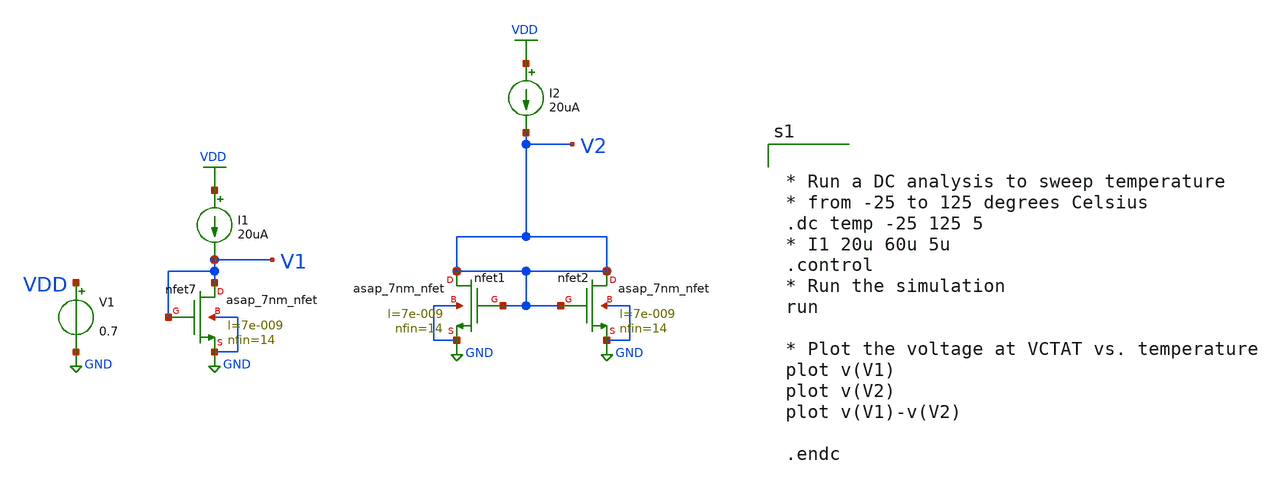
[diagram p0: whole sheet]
** sch_path: xschem/Circuits/PTAT_IDEAL_CURRENT_SOURCE.sch
* AsahiroKenpachi/asap_7nm_Xschem/asap_7nm_nfet.sym:
* Copyright 2021 Stefan Frederik Schippers
* Licensed under the Apache License, Version 2.0 (the "License");
**.subckt PTAT_IDEAL_CURRENT_SOURCE
I1 VDD V1 20uA
V1 VDD GND 0.7
Xnfet7 V1 V1 GND GND asap_7nm_nfet l=7e-009 nfin=14
I2 VDD V2 20uA
Xnfet1 V2 V2 GND GND asap_7nm_nfet l=7e-009 nfin=14
Xnfet2 V2 V2 GND GND asap_7nm_nfet l=7e-009 nfin=14
**** begin user architecture code


* Run a DC analysis to sweep temperature
* from -25 to 125 degrees Celsius
.dc temp -25 125 5
* I1 20u 60u 5u
.control
* Run the simulation
run

* Plot the voltage at VCTAT vs. temperature
plot v(V1)
plot v(V2)
plot v(V1)-v(V2)

.endc


**** end user architecture code
**.ends
.GLOBAL VDD
.GLOBAL GND
**** begin user architecture code

.subckt asap_7nm_nfet S G D B l=@l nfin=@nfin
	nnmos_finfet S G D B BSIMCMG_osdi_N l=@l nfin=@nfin
.ends asap_7nm_nfet

.model BSIMCMG_osdi_N BSIMCMG_va (  TYPE = 1
************************************************************
*                         general                          *
************************************************************ version = 107             bulkmod = 1
*+               igcmod  = 1               igbmod  = 0              gidlmod = 1               iimod   = 0
*+               geomod  = 1               rdsmod  = 0              rgatemod= 0               rgeomod = 0
*+               shmod   = 0               nqsmod  = 0              coremod = 0               cgeomod = 0
*+               capmod  = 0               tnom    = 25             eot     = 1e-009          eotbox  = 1.4e-007
*+        eotacc  = 1e-010          tfin    = 6.5e-009       toxp    = 2.1e-009        nbody   = 1e+022
*+          phig    = 4.2466          epsrox  = 3.9            epsrsub = 11.9            easub   = 4.05
*+            ni0sub  = 1.1e+016        bg0sub  = 1.17           nc0sub  = 2.86e+025       nsd     = 2e+026
*+          ngate   = 0               nseg    = 5              l       = 2.1e-008        xl      = 1e-009
*+          lint    = -2e-009         dlc     = 0              dlbin   = 0               hfin    = 3.2e-008
*+        deltaw  = 0               deltawcv= 0              sdterm  = 0               epsrsp  = 3.9
*+             nfin    = 1 toxg    = 1.80e-009
************************************************************
*                            dc                            *
************************************************************ cit     = 0               cdsc    =
*+ 0.01            cdscd   = 0.01            dvt0    = 0.05           dvt1    = 0.47            phin    =
*+ 0.05            eta0    = 0.07            dsub    = 0.35           k1rsce  = 0               lpe0    = 0
*+               dvtshift= 0               qmfactor= 2.5            etaqm   = 0.54            qm0     = 0.001           pqm
*+     = 0.66            u0      = 0.0303         etamob  = 2               up      = 0               ua
*+      = 0.55            eu      = 1.2            ud      = 0               ucs     = 1
*+               rdswmin = 0               rdsw    = 200            wr      = 1               rswmin  = 0
*+               rdwmin  = 0               rshs    = 0              rshd    = 0               vsat    = 70000
*+           deltavsat= 0.2             ksativ  = 2              mexp    = 4               ptwg    = 30              pclm
*+    = 0.05            pclmg   = 0              pdibl1  = 0               pdibl2  = 0.002           drout
*+   = 1               pvag    = 0              fpitch  = 2.7e-008        rth0    = 0.225           cth0
*+    = 1.243e-006      wth0    = 2.6e-007       lcdscd  = 5e-005          lcdscdr = 5e-005          lrdsw
*+   = 0.2             lvsat   = 0
************************************************************
*                         leakage                          *
************************************************************ aigc    = 0.014           bigc    =
*+ 0.005           cigc    = 0.25            dlcigs  = 1e-009         dlcigd  = 1e-009          aigs    =
*+ 0.0115          aigd    = 0.0115          bigs    = 0.00332        bigd    = 0.00332         cigs    =
*+ 0.35            cigd    = 0.35            poxedge = 1.1            agidl   = 1e-012          agisl   =
*+ 1e-012          bgidl   = 10000000        bgisl   = 10000000       egidl   = 0.35            egisl   =
*+ 0.35
************************************************************
*                            rf                            *
************************************************************
************************************************************
*                         junction                         *
************************************************************
************************************************************
*                       capacitance                        *
************************************************************ cfs     = 0               cfd     = 0
*+               cgso    = 1.6e-010        cgdo    = 1.6e-010       cgsl    = 0               cgdl    = 0
*+               ckappas = 0.6             ckappad = 0.6            cgbo    = 0               cgbl    = 0
************************************************************
*                       temperature                        *
************************************************************ tbgasub = 0.000473        tbgbsub = 636
*+             kt1     = 0               kt1l    = 0              ute     = -0.7            utl     = 0
*+               ua1     = 0.001032        ud1     = 0              ucste   = -0.004775       at      = 0.001
*+           ptwgt   = 0.004           tmexp   = 0              prt     = 0               tgidl   = -0.007
*+          igt     = 2.5
************************************************************
*                          noise                           *
************************************************************
**)
.control
pre_osdi /home/hprcse/Documents/test/bsimcmg.osdi
.endc


**** end user architecture code
.end
